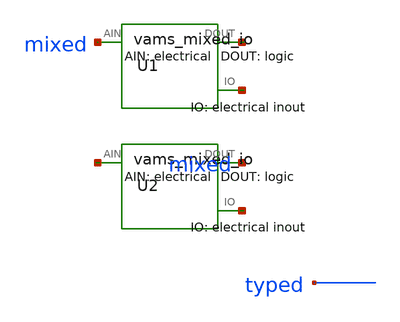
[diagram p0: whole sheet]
** sch_path: xschem_library/devices/vams_mixed_net.sch
**.subckt vams_mixed_net
**.ends

* expanding   symbol:  vams_mixed_io.sym # of pins=3
** sym_path: xschem_library/devices/vams_mixed_io.sym
** sch_path: xschem_library/devices/vams_mixed_io.sch
.subckt vams_mixed_io
*.iopin IO
*.ipin AIN
*.opin DOUT
R1 IO AIN 1k m=1
A1 [ AIN ] [ DOUT ] adc_buff
.ends

.end
